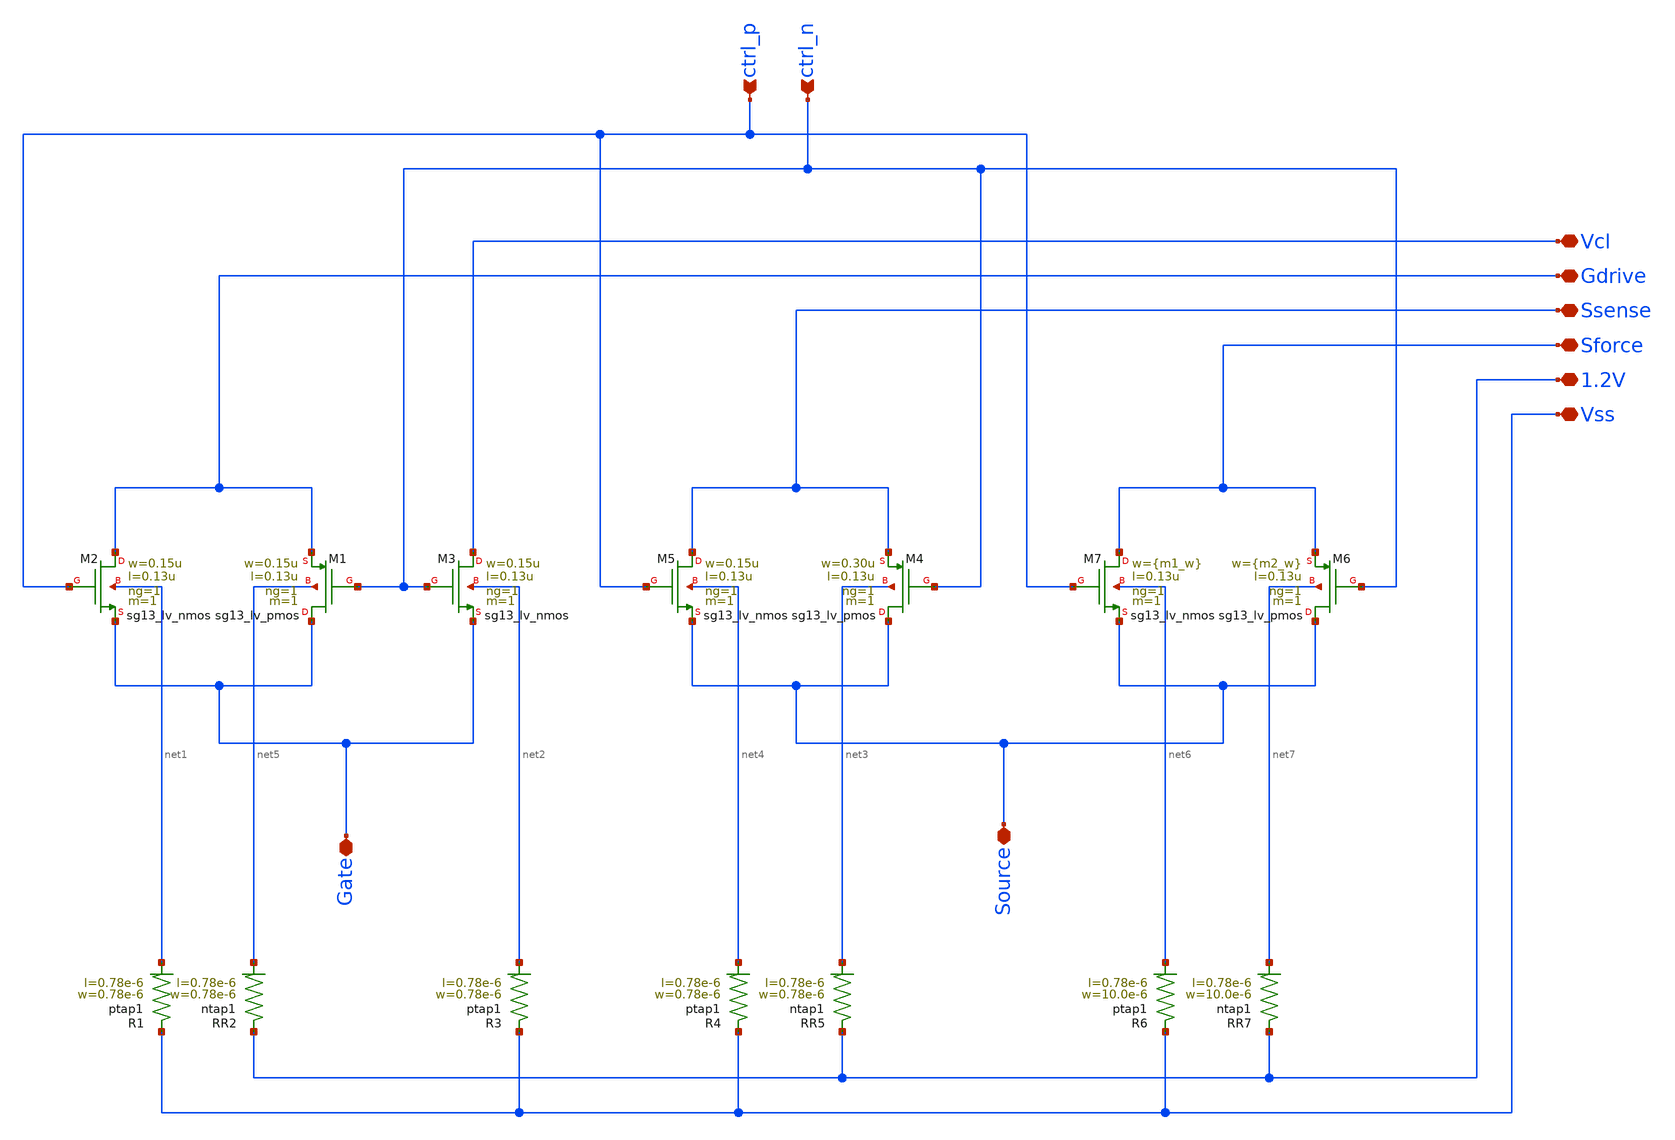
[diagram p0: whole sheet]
** sch_path: design_data/xschem/new_tb/Gate_Line.sch
**.subckt Gate_Line Gate Vss Gdrive ctrl_p 1.2V Vcl Ssense Source Sforce ctrl_n
*.iopin Gate
*.iopin Vss
*.iopin Gdrive
*.ipin ctrl_p
*.iopin 1.2V
*.iopin Vcl
*.iopin Ssense
*.iopin Source
*.iopin Sforce
*.ipin ctrl_n
XM1 Gate ctrl_n Gdrive net5 sg13_lv_pmos w=0.15u l=0.13u ng=1 m=1 mm_ok=1
XM2 Gdrive ctrl_p Gate net1 sg13_lv_nmos w=0.15u l=0.13u ng=1 m=1 mm_ok=1
XM3 Vcl ctrl_n Gate net2 sg13_lv_nmos w=0.15u l=0.13u ng=1 m=1 mm_ok=1
XM4 Source ctrl_n Ssense net3 sg13_lv_pmos w=0.30u l=0.13u ng=1 m=1 mm_ok=1
XM5 Ssense ctrl_p Source net4 sg13_lv_nmos w=0.15u l=0.13u ng=1 m=1 mm_ok=1
XM6 Source ctrl_n Sforce net7 sg13_lv_pmos w={m2_w} l=0.13u ng=1 m=1 mm_ok=1
XM7 Sforce ctrl_p Source net6 sg13_lv_nmos w={m1_w} l=0.13u ng=1 m=1 mm_ok=1
XR1 Vss net1 ptap1 R=262.8 w=0.78e-6 l=0.78e-6
XR2 1.2V net5 ntap1 R=262.8 w=0.78e-6 l=0.78e-6
XR3 Vss net2 ptap1 R=262.8 w=0.78e-6 l=0.78e-6
XR4 Vss net4 ptap1 R=262.8 w=0.78e-6 l=0.78e-6
XR5 1.2V net3 ntap1 R=262.8 w=0.78e-6 l=0.78e-6
XR6 Vss net6 ptap1 R=33.38 w=10.0e-6 l=0.78e-6
XR7 1.2V net7 ntap1 R=33.38 w=10.0e-6 l=0.78e-6
**.ends
.end
